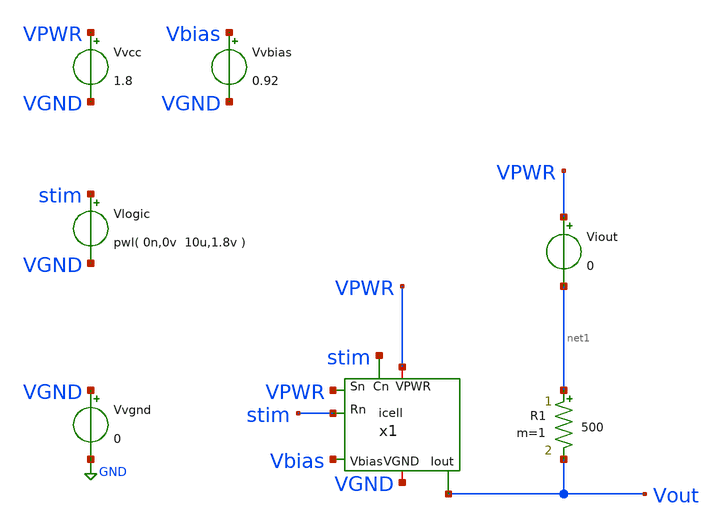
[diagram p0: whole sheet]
** sch_path: xschem/tb_icell.sch
**.subckt tb_icell
x1 VPWR VGND stim stim VPWR Vbias Vout icell
Vvcc VPWR VGND 1.8
R1 net1 Vout 500 m=1
Vvbias Vbias VGND 0.92
Vvgnd VGND GND 0
Viout VPWR net1 0
Vlogic stim VGND pwl( 0n,0v 10u,1.8v )
**** begin user architecture code



.options savecurrents
.control

    save all
    tran 1n 12.8u
    write tb_icell.raw vout

.endc




.lib $::SKYWATER_MODELS/sky130.lib.spice tt
.include $::SKYWATER_STDCELLS/sky130_fd_sc_hd.spice

**** end user architecture code
**.ends

* expanding   symbol:  icell.sym # of pins=7
** sym_path: xschem/icell.sym
** sch_path: xschem/icell.sch
.subckt icell VPWR VGND Rn Cn Sn Vbias Iout
*.ipin Rn
*.iopin VPWR
*.opin Iout
*.iopin VGND
*.ipin Cn
*.ipin Sn
*.ipin Vbias
XMsp Ien Sn VPWR VPWR sky130_fd_pr__pfet_01v8 L=0.15 W=0.5 nf=1 ad='int((nf+1)/2) * W/nf * 0.29' as='int((nf+2)/2) * W/nf * 0.29'
+ pd='2*int((nf+1)/2) * (W/nf + 0.29)' ps='2*int((nf+2)/2) * (W/nf + 0.29)' nrd='0.29 / W' nrs='0.29 / W'
+ sa=0 sb=0 sd=0 mult=1 m=1
XMsna Ien Sn PDM VGND sky130_fd_pr__nfet_01v8 L=0.15 W=0.5 nf=1 ad='int((nf+1)/2) * W/nf * 0.29' as='int((nf+2)/2) * W/nf * 0.29'
+ pd='2*int((nf+1)/2) * (W/nf + 0.29)' ps='2*int((nf+2)/2) * (W/nf + 0.29)' nrd='0.29 / W' nrs='0.29 / W'
+ sa=0 sb=0 sd=0 mult=1 m=1
XMcpa Ien Cn PUM VPWR sky130_fd_pr__pfet_01v8 L=0.15 W=0.5 nf=1 ad='int((nf+1)/2) * W/nf * 0.29' as='int((nf+2)/2) * W/nf * 0.29'
+ pd='2*int((nf+1)/2) * (W/nf + 0.29)' ps='2*int((nf+2)/2) * (W/nf + 0.29)' nrd='0.29 / W' nrs='0.29 / W'
+ sa=0 sb=0 sd=0 mult=1 m=1
XMrpa PUM Rn VPWR VPWR sky130_fd_pr__pfet_01v8 L=0.15 W=0.5 nf=1 ad='int((nf+1)/2) * W/nf * 0.29' as='int((nf+2)/2) * W/nf * 0.29'
+ pd='2*int((nf+1)/2) * (W/nf + 0.29)' ps='2*int((nf+2)/2) * (W/nf + 0.29)' nrd='0.29 / W' nrs='0.29 / W'
+ sa=0 sb=0 sd=0 mult=1 m=1
XMrno PDM Rn VGND VGND sky130_fd_pr__nfet_01v8 L=0.15 W=0.5 nf=1 ad='int((nf+1)/2) * W/nf * 0.29' as='int((nf+2)/2) * W/nf * 0.29'
+ pd='2*int((nf+1)/2) * (W/nf + 0.29)' ps='2*int((nf+2)/2) * (W/nf + 0.29)' nrd='0.29 / W' nrs='0.29 / W'
+ sa=0 sb=0 sd=0 mult=1 m=1
XMcno PDM Cn VGND VGND sky130_fd_pr__nfet_01v8 L=0.15 W=0.5 nf=1 ad='int((nf+1)/2) * W/nf * 0.29' as='int((nf+2)/2) * W/nf * 0.29'
+ pd='2*int((nf+1)/2) * (W/nf + 0.29)' ps='2*int((nf+2)/2) * (W/nf + 0.29)' nrd='0.29 / W' nrs='0.29 / W'
+ sa=0 sb=0 sd=0 mult=1 m=1
XMiu SM Vbias VGND VGND sky130_fd_pr__nfet_g5v0d10v5 L=0.5 W=0.5 nf=1 ad='int((nf+1)/2) * W/nf * 0.29'
+ as='int((nf+2)/2) * W/nf * 0.29' pd='2*int((nf+1)/2) * (W/nf + 0.29)' ps='2*int((nf+2)/2) * (W/nf + 0.29)'
+ nrd='0.29 / W' nrs='0.29 / W' sa=0 sb=0 sd=0 mult=1 m=1
XMsw Iout Ien SM VGND sky130_fd_pr__nfet_g5v0d10v5 L=0.5 W=0.5 nf=1 ad='int((nf+1)/2) * W/nf * 0.29'
+ as='int((nf+2)/2) * W/nf * 0.29' pd='2*int((nf+1)/2) * (W/nf + 0.29)' ps='2*int((nf+2)/2) * (W/nf + 0.29)'
+ nrd='0.29 / W' nrs='0.29 / W' sa=0 sb=0 sd=0 mult=1 m=1
.ends

.GLOBAL GND
.end
